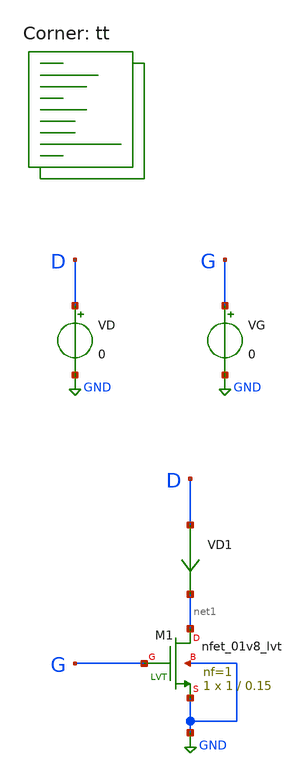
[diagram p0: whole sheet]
** sch_path: projects/pll/trials/tut1.sch
**.subckt tut1
XM1 net1 G GND GND sky130_fd_pr__nfet_01v8_lvt L=0.15 W=1 nf=1 ad='int((nf+1)/2) * W/nf * 0.29' as='int((nf+2)/2) * W/nf * 0.29'
+ pd='2*int((nf+1)/2) * (W/nf + 0.29)' ps='2*int((nf+2)/2) * (W/nf + 0.29)' nrd='0.29 / W' nrs='0.29 / W'
+ sa=0 sb=0 sd=0 mult=1 m=1
VD1 D net1 0
.save i(vd1)
VD D GND 0
VG G GND 0
**** begin user architecture code



.control
save all
dc VD 0 2 0.01 VG 0 2 0.2
write tut1.raw
.endc



.lib $::SKYWATER_MODELS/sky130.lib.spice tt
**** end user architecture code
**.ends
.GLOBAL GND
.end
